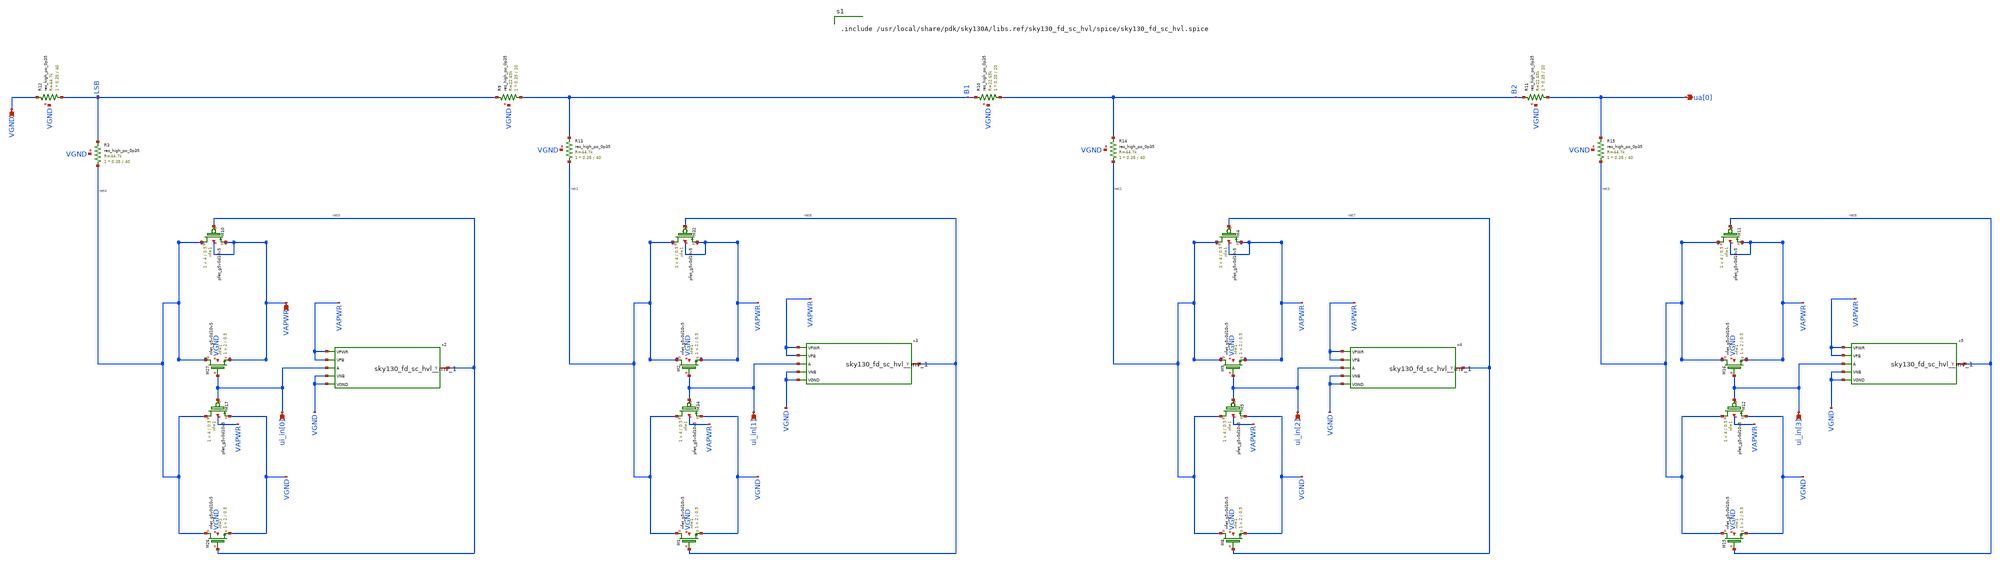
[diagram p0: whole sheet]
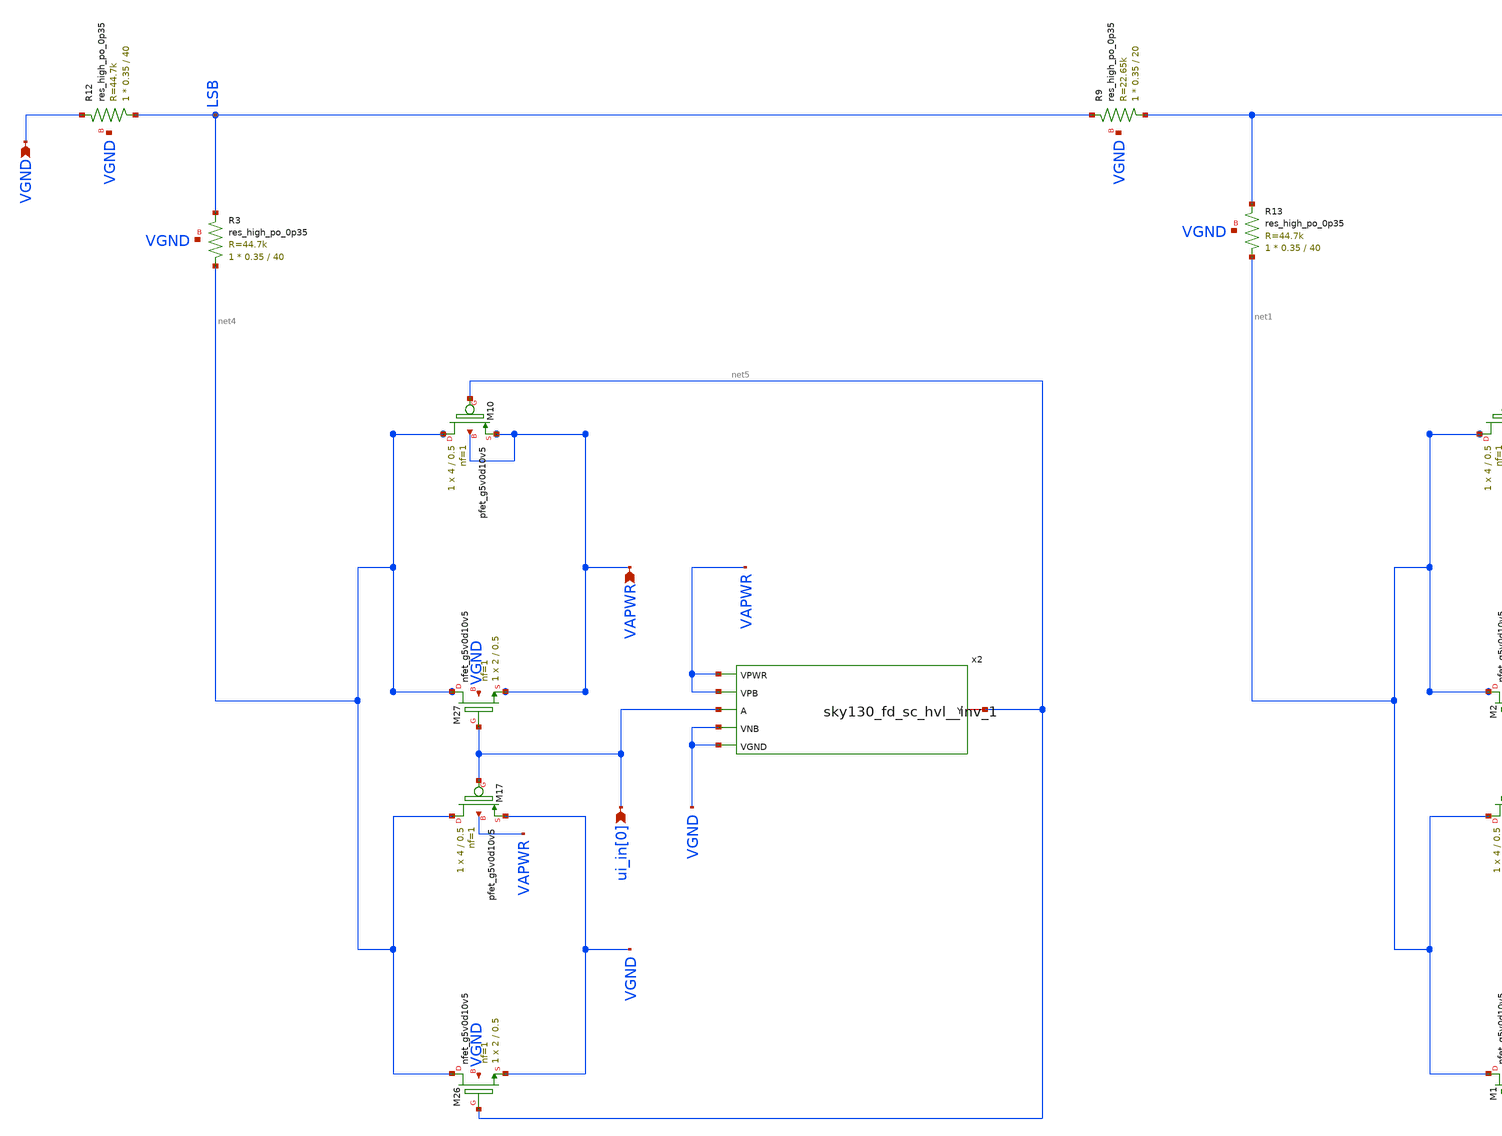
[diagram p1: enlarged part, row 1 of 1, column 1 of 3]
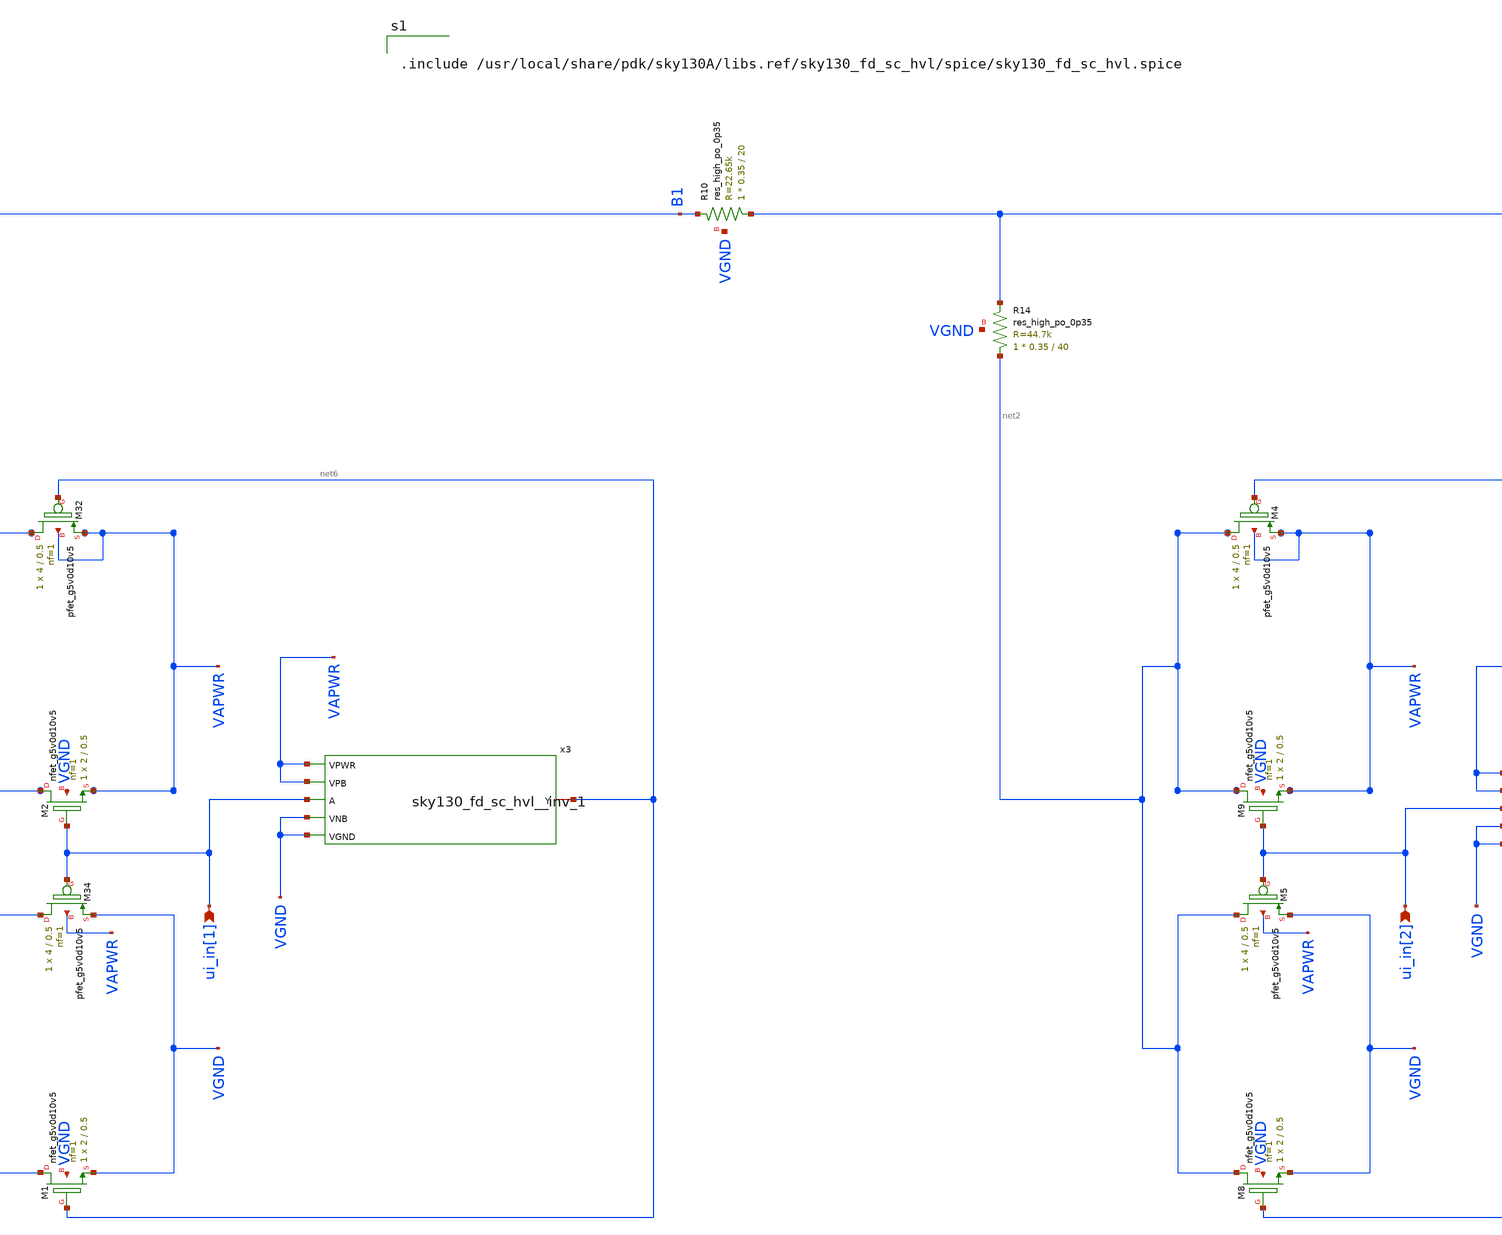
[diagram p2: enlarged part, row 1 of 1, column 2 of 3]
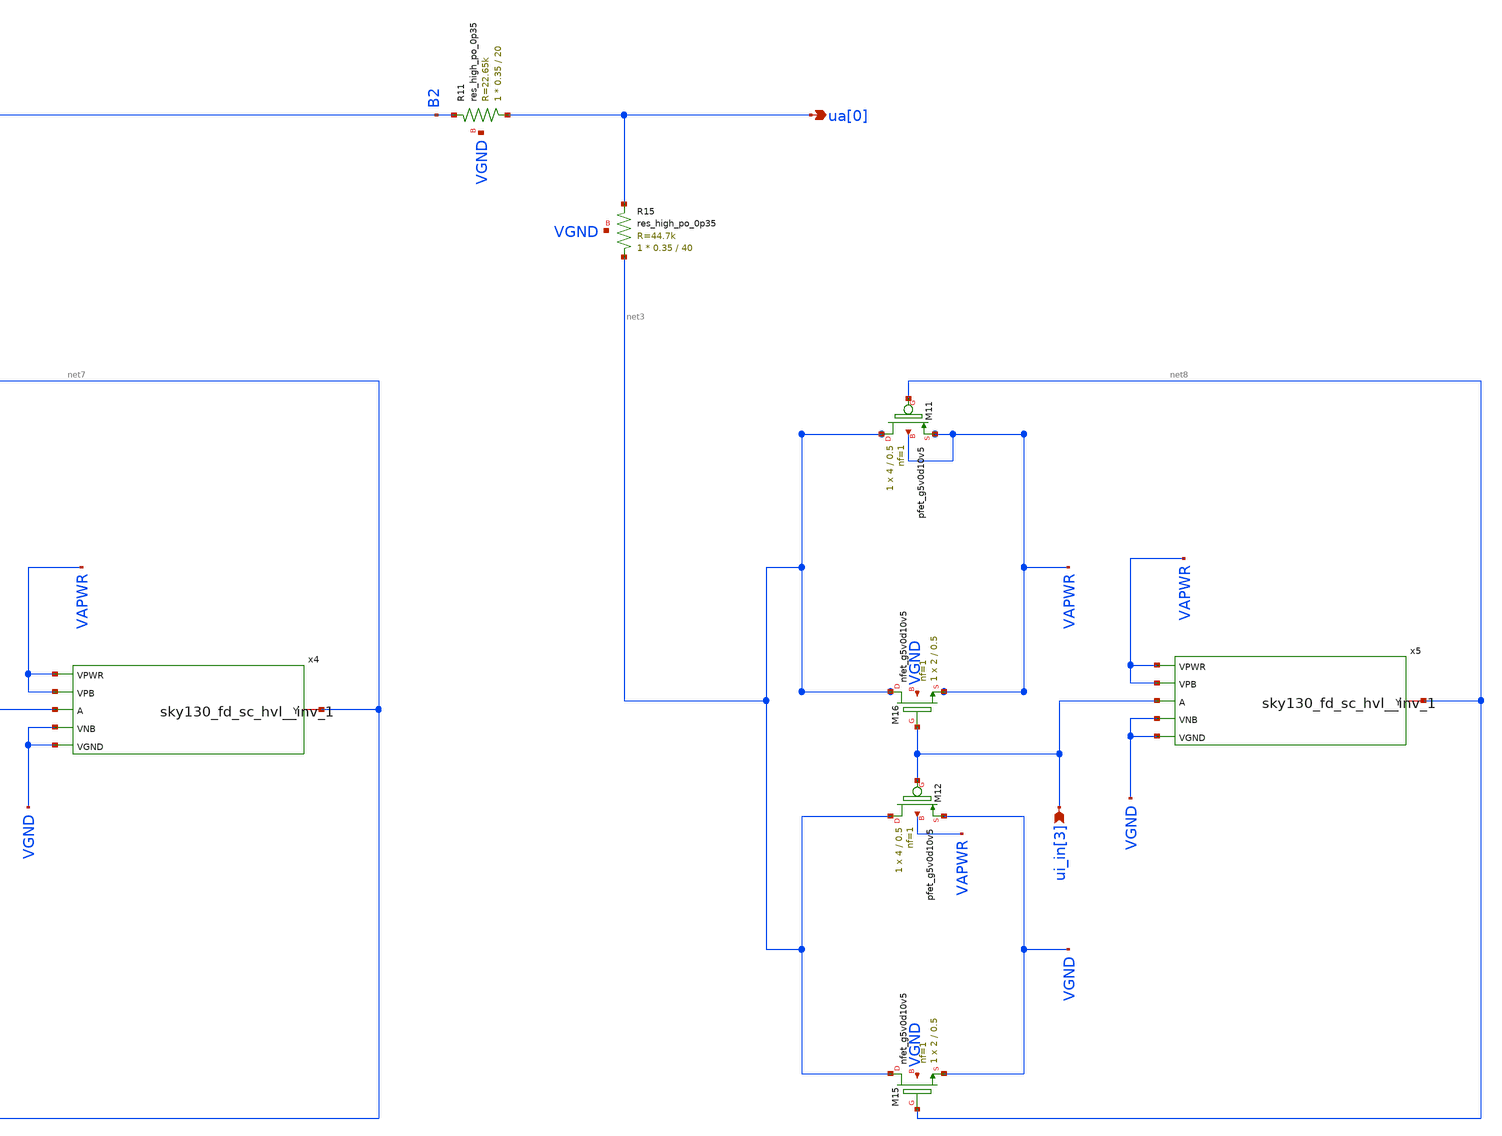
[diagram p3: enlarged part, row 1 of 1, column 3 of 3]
** sch_path: xschem/dac_lvs.sch
**.subckt dac_lvs ua[0] VGND ui_in[0] ui_in[1] ui_in[2] ui_in[3] VAPWR
*.opin ua[0]
*.ipin VGND
*.ipin ui_in[0]
*.ipin ui_in[1]
*.ipin ui_in[2]
*.ipin ui_in[3]
*.ipin VAPWR
XM10 net4 net5 VAPWR VAPWR sky130_fd_pr__pfet_g5v0d10v5 L=0.5 W=4 nf=1 ad=0 as=0 pd=0 ps=0 nrd=0
+ nrs=0 sa=0 sb=0 sd=0 mult=1 m=1
XM17 net4 ui_in[0] VGND VAPWR sky130_fd_pr__pfet_g5v0d10v5 L=0.5 W=4 nf=1 ad=0 as=0 pd=0 ps=0 nrd=0
+ nrs=0 sa=0 sb=0 sd=0 mult=1 m=1
XM26 net4 net5 VGND VGND sky130_fd_pr__nfet_g5v0d10v5 L=0.5 W=2 nf=1 ad=0 as=0 pd=0 ps=0 nrd=0 nrs=0
+ sa=0 sb=0 sd=0 mult=1 m=1
XM27 net4 ui_in[0] VAPWR VGND sky130_fd_pr__nfet_g5v0d10v5 L=0.5 W=2 nf=1 ad=0 as=0 pd=0 ps=0 nrd=0
+ nrs=0 sa=0 sb=0 sd=0 mult=1 m=1
XM32 net1 net6 VAPWR VAPWR sky130_fd_pr__pfet_g5v0d10v5 L=0.5 W=4 nf=1 ad=0 as=0 pd=0 ps=0 nrd=0
+ nrs=0 sa=0 sb=0 sd=0 mult=1 m=1
XM34 net1 ui_in[1] VGND VAPWR sky130_fd_pr__pfet_g5v0d10v5 L=0.5 W=4 nf=1 ad=0 as=0 pd=0 ps=0 nrd=0
+ nrs=0 sa=0 sb=0 sd=0 mult=1 m=1
XM1 net1 net6 VGND VGND sky130_fd_pr__nfet_g5v0d10v5 L=0.5 W=2 nf=1 ad=0 as=0 pd=0 ps=0 nrd=0 nrs=0
+ sa=0 sb=0 sd=0 mult=1 m=1
XM2 net1 ui_in[1] VAPWR VGND sky130_fd_pr__nfet_g5v0d10v5 L=0.5 W=2 nf=1 ad=0 as=0 pd=0 ps=0 nrd=0
+ nrs=0 sa=0 sb=0 sd=0 mult=1 m=1
XM4 net2 net7 VAPWR VAPWR sky130_fd_pr__pfet_g5v0d10v5 L=0.5 W=4 nf=1 ad=0 as=0 pd=0 ps=0 nrd=0
+ nrs=0 sa=0 sb=0 sd=0 mult=1 m=1
XM5 net2 ui_in[2] VGND VAPWR sky130_fd_pr__pfet_g5v0d10v5 L=0.5 W=4 nf=1 ad=0 as=0 pd=0 ps=0 nrd=0
+ nrs=0 sa=0 sb=0 sd=0 mult=1 m=1
XM8 net2 net7 VGND VGND sky130_fd_pr__nfet_g5v0d10v5 L=0.5 W=2 nf=1 ad=0 as=0 pd=0 ps=0 nrd=0 nrs=0
+ sa=0 sb=0 sd=0 mult=1 m=1
XM9 net2 ui_in[2] VAPWR VGND sky130_fd_pr__nfet_g5v0d10v5 L=0.5 W=2 nf=1 ad=0 as=0 pd=0 ps=0 nrd=0
+ nrs=0 sa=0 sb=0 sd=0 mult=1 m=1
XM11 net3 net8 VAPWR VAPWR sky130_fd_pr__pfet_g5v0d10v5 L=0.5 W=4 nf=1 ad=0 as=0 pd=0 ps=0 nrd=0
+ nrs=0 sa=0 sb=0 sd=0 mult=1 m=1
XM12 net3 ui_in[3] VGND VAPWR sky130_fd_pr__pfet_g5v0d10v5 L=0.5 W=4 nf=1 ad=0 as=0 pd=0 ps=0 nrd=0
+ nrs=0 sa=0 sb=0 sd=0 mult=1 m=1
XM15 net3 net8 VGND VGND sky130_fd_pr__nfet_g5v0d10v5 L=0.5 W=2 nf=1 ad=0 as=0 pd=0 ps=0 nrd=0 nrs=0
+ sa=0 sb=0 sd=0 mult=1 m=1
XM16 net3 ui_in[3] VAPWR VGND sky130_fd_pr__nfet_g5v0d10v5 L=0.5 W=2 nf=1 ad=0 as=0 pd=0 ps=0 nrd=0
+ nrs=0 sa=0 sb=0 sd=0 mult=1 m=1
XR10 B2 B1 VGND sky130_fd_pr__res_high_po_0p35 L=20 mult=1 m=1
XR9 B1 LSB VGND sky130_fd_pr__res_high_po_0p35 L=20 mult=1 m=1
XR11 ua[0] B2 VGND sky130_fd_pr__res_high_po_0p35 L=20 mult=1 m=1
XR12 LSB VGND VGND sky130_fd_pr__res_high_po_0p35 L=40 mult=1 m=1
XR13 net1 B1 VGND sky130_fd_pr__res_high_po_0p35 L=40 mult=1 m=1
XR14 net2 B2 VGND sky130_fd_pr__res_high_po_0p35 L=40 mult=1 m=1
XR15 net3 ua[0] VGND sky130_fd_pr__res_high_po_0p35 L=40 mult=1 m=1
XR3 net4 LSB VGND sky130_fd_pr__res_high_po_0p35 L=40 mult=1 m=1
x2 ui_in[0] VGND VGND VAPWR VAPWR net5 sky130_fd_sc_hvl__inv_1
x3 ui_in[1] VGND VGND VAPWR VAPWR net6 sky130_fd_sc_hvl__inv_1
x4 ui_in[2] VGND VGND VAPWR VAPWR net7 sky130_fd_sc_hvl__inv_1
x5 ui_in[3] VGND VGND VAPWR VAPWR net8 sky130_fd_sc_hvl__inv_1
**** begin user architecture code


.include /usr/local/share/pdk/sky130A/libs.ref/sky130_fd_sc_hvl/spice/sky130_fd_sc_hvl.spice


**** end user architecture code
**.ends
.end
